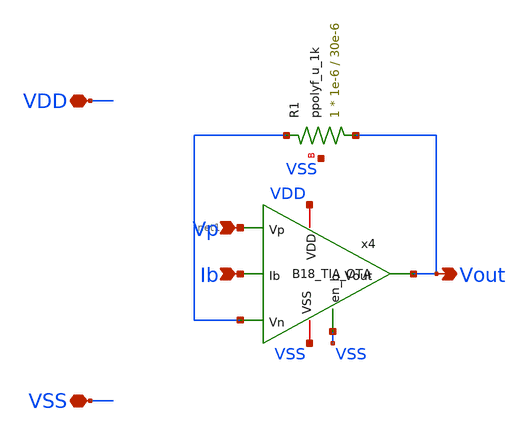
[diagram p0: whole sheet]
** sch_path: Analog/schematics/1_readout/tia/B18_TIA.sch
**.subckt B18_TIA VDD VSS Vp Ib Vout
*.iopin VDD
*.iopin VSS
*.ipin Vp
*.ipin Ib
*.opin Vout
x4 Vp net1 Vout VDD VSS Ib VSS B18_TIA_OTA
XR1 Vout net1 VSS ppolyf_u_1k r_width=1e-6 r_length=30e-6 m=1
**.ends

* expanding   symbol:  /workspace/Probton/Analog/schematics/1_readout/tia/B18_TIA_OTA.sym # of
*+ pins=7
** sym_path: Analog/schematics/1_readout/tia/B18_TIA_OTA.sym
** sch_path: Analog/schematics/1_readout/tia/B18_TIA_OTA.sch
.subckt B18_TIA_OTA Vp Vn Vout VDD VSS Ib en_b
*.ipin Vp
*.ipin Vn
*.opin Vout
*.iopin VDD
*.iopin VSS
*.ipin Ib
*.ipin en_b
XMP_MIR_NEG Vout net1 VDD VDD pfet_03v3 L=0.5u W=70u nf=14 ad='int((nf+1)/2) * W/nf * 0.18u' as='int((nf+2)/2) * W/nf * 0.18u'
+ pd='2*int((nf+1)/2) * (W/nf + 0.18u)' ps='2*int((nf+2)/2) * (W/nf + 0.18u)' nrd='0.18u / W' nrs='0.18u / W'
+ sa=0 sb=0 sd=0 m=1
XMP_MIR_POS net1 net1 VDD VDD pfet_03v3 L=0.5u W=70u nf=14 ad='int((nf+1)/2) * W/nf * 0.18u' as='int((nf+2)/2) * W/nf * 0.18u'
+ pd='2*int((nf+1)/2) * (W/nf + 0.18u)' ps='2*int((nf+2)/2) * (W/nf + 0.18u)' nrd='0.18u / W' nrs='0.18u / W'
+ sa=0 sb=0 sd=0 m=1
XMN_IN_POS net1 Vp net2 VSS nfet_03v3 L=0.5u W=20u nf=4 ad='int((nf+1)/2) * W/nf * 0.18u' as='int((nf+2)/2) * W/nf * 0.18u'
+ pd='2*int((nf+1)/2) * (W/nf + 0.18u)' ps='2*int((nf+2)/2) * (W/nf + 0.18u)' nrd='0.18u / W' nrs='0.18u / W'
+ sa=0 sb=0 sd=0 m=1
XMN_IN_NEG Vout Vn net2 VSS nfet_03v3 L=0.5u W=20u nf=4 ad='int((nf+1)/2) * W/nf * 0.18u' as='int((nf+2)/2) * W/nf * 0.18u'
+ pd='2*int((nf+1)/2) * (W/nf + 0.18u)' ps='2*int((nf+2)/2) * (W/nf + 0.18u)' nrd='0.18u / W' nrs='0.18u / W'
+ sa=0 sb=0 sd=0 m=1
XMN_TAIL net2 Ib VSS VSS nfet_03v3 L=0.5u W=40u nf=8 ad='int((nf+1)/2) * W/nf * 0.18u' as='int((nf+2)/2) * W/nf * 0.18u'
+ pd='2*int((nf+1)/2) * (W/nf + 0.18u)' ps='2*int((nf+2)/2) * (W/nf + 0.18u)' nrd='0.18u / W' nrs='0.18u / W'
+ sa=0 sb=0 sd=0 m=1
XMN_TAILMIR Ib Ib VSS VSS nfet_03v3 L=0.5u W=40u nf=8 ad='int((nf+1)/2) * W/nf * 0.18u' as='int((nf+2)/2) * W/nf * 0.18u'
+ pd='2*int((nf+1)/2) * (W/nf + 0.18u)' ps='2*int((nf+2)/2) * (W/nf + 0.18u)' nrd='0.18u / W' nrs='0.18u / W'
+ sa=0 sb=0 sd=0 m=1
XMN_SWITCH Ib en_b VSS VSS nfet_03v3 L=0.5u W=1u nf=1 ad='int((nf+1)/2) * W/nf * 0.18u' as='int((nf+2)/2) * W/nf * 0.18u'
+ pd='2*int((nf+1)/2) * (W/nf + 0.18u)' ps='2*int((nf+2)/2) * (W/nf + 0.18u)' nrd='0.18u / W' nrs='0.18u / W'
+ sa=0 sb=0 sd=0 m=1
**** begin user architecture code


* B18_TIA_OTA

* Original Design Specifications:
  * gm_id for all transistors is 12 V^-1 (moderate inversion)
  * C_L = 2pF
  * GBW = 50MHz
  * L = 0.5um

* Results using pygmid:

*             MN_TAIL  MN_IN   MP_MIR

*  W(um)      38.5     19.25   66.52
*  nf@W=5um   8        4       14
*  Id(uA)     105      52.4    52.4



* The enable signal is a simple NMOS gate pulldown transistor
* placed at the tail current mirror. Assuming a digital signal
* of 3.3V is present, the active-low switch will turn off the
* current mirror


**** end user architecture code
.ends

.end
